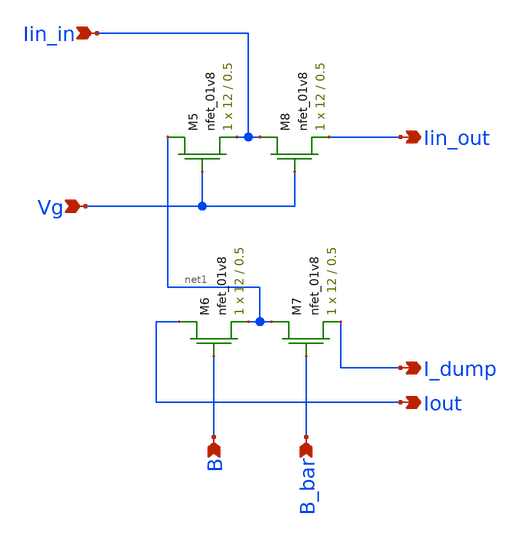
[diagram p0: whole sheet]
** sch_path: ladder_1bit.sch
**.subckt ladder_1bit Iin_in Vg B B_bar Iin_out I_dump Iout
*.ipin Iin_in
*.ipin Vg
*.ipin B
*.ipin B_bar
*.opin Iin_out
*.opin I_dump
*.opin Iout
XM5 net1 Vg Iin_in GND sky130_fd_pr__nfet_01v8 L=0.5 W=12 nf=1 ad='int((nf+1)/2) * W/nf * 0.29' as='int((nf+2)/2) * W/nf * 0.29'
+ pd='2*int((nf+1)/2) * (W/nf + 0.29)' ps='2*int((nf+2)/2) * (W/nf + 0.29)' nrd='0.29 / W' nrs='0.29 / W'
+ sa=0 sb=0 sd=0 mult=1 m=1
XM6 Iout B net1 GND sky130_fd_pr__nfet_01v8 L=0.5 W=12 nf=1 ad='int((nf+1)/2) * W/nf * 0.29' as='int((nf+2)/2) * W/nf * 0.29'
+ pd='2*int((nf+1)/2) * (W/nf + 0.29)' ps='2*int((nf+2)/2) * (W/nf + 0.29)' nrd='0.29 / W' nrs='0.29 / W'
+ sa=0 sb=0 sd=0 mult=1 m=1
XM7 net1 B_bar I_dump GND sky130_fd_pr__nfet_01v8 L=0.5 W=12 nf=1 ad='int((nf+1)/2) * W/nf * 0.29' as='int((nf+2)/2) * W/nf * 0.29'
+ pd='2*int((nf+1)/2) * (W/nf + 0.29)' ps='2*int((nf+2)/2) * (W/nf + 0.29)' nrd='0.29 / W' nrs='0.29 / W'
+ sa=0 sb=0 sd=0 mult=1 m=1
XM8 Iin_in Vg Iin_out GND sky130_fd_pr__nfet_01v8 L=0.5 W=12 nf=1 ad='int((nf+1)/2) * W/nf * 0.29' as='int((nf+2)/2) * W/nf * 0.29'
+ pd='2*int((nf+1)/2) * (W/nf + 0.29)' ps='2*int((nf+2)/2) * (W/nf + 0.29)' nrd='0.29 / W' nrs='0.29 / W'
+ sa=0 sb=0 sd=0 mult=1 m=1
**.ends
.end
